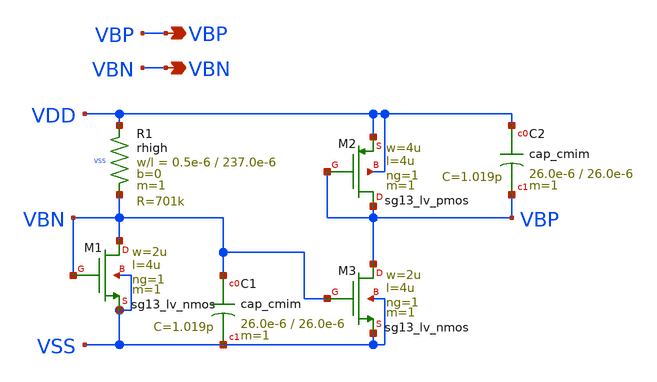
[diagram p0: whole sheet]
** sch_path: design/blocks/bias/schematic/bias.sch
**.subckt bias VBP VBN
*.opin VBP
*.opin VBN
XM1 VBN VBN VSS VSS sg13_lv_nmos w=2u l=4u ng=1 m=1 mm_ok=1
XM2 VBP VBP VDD VDD sg13_lv_pmos w=4u l=4u ng=1 m=1 mm_ok=1
XR1 VDD VBN VSS rhigh w=0.5e-6 l=237.0e-6 m=1 b=0 mm_ok=1
XC1 VBN VSS cap_cmim w=26.0e-6 l=26.0e-6 m=1 mm_ok=1
XC2 VDD VBP cap_cmim w=26.0e-6 l=26.0e-6 m=1 mm_ok=1
XM3 VBP VBN VSS VSS sg13_lv_nmos w=2u l=4u ng=1 m=1 mm_ok=1
**.ends
.end
